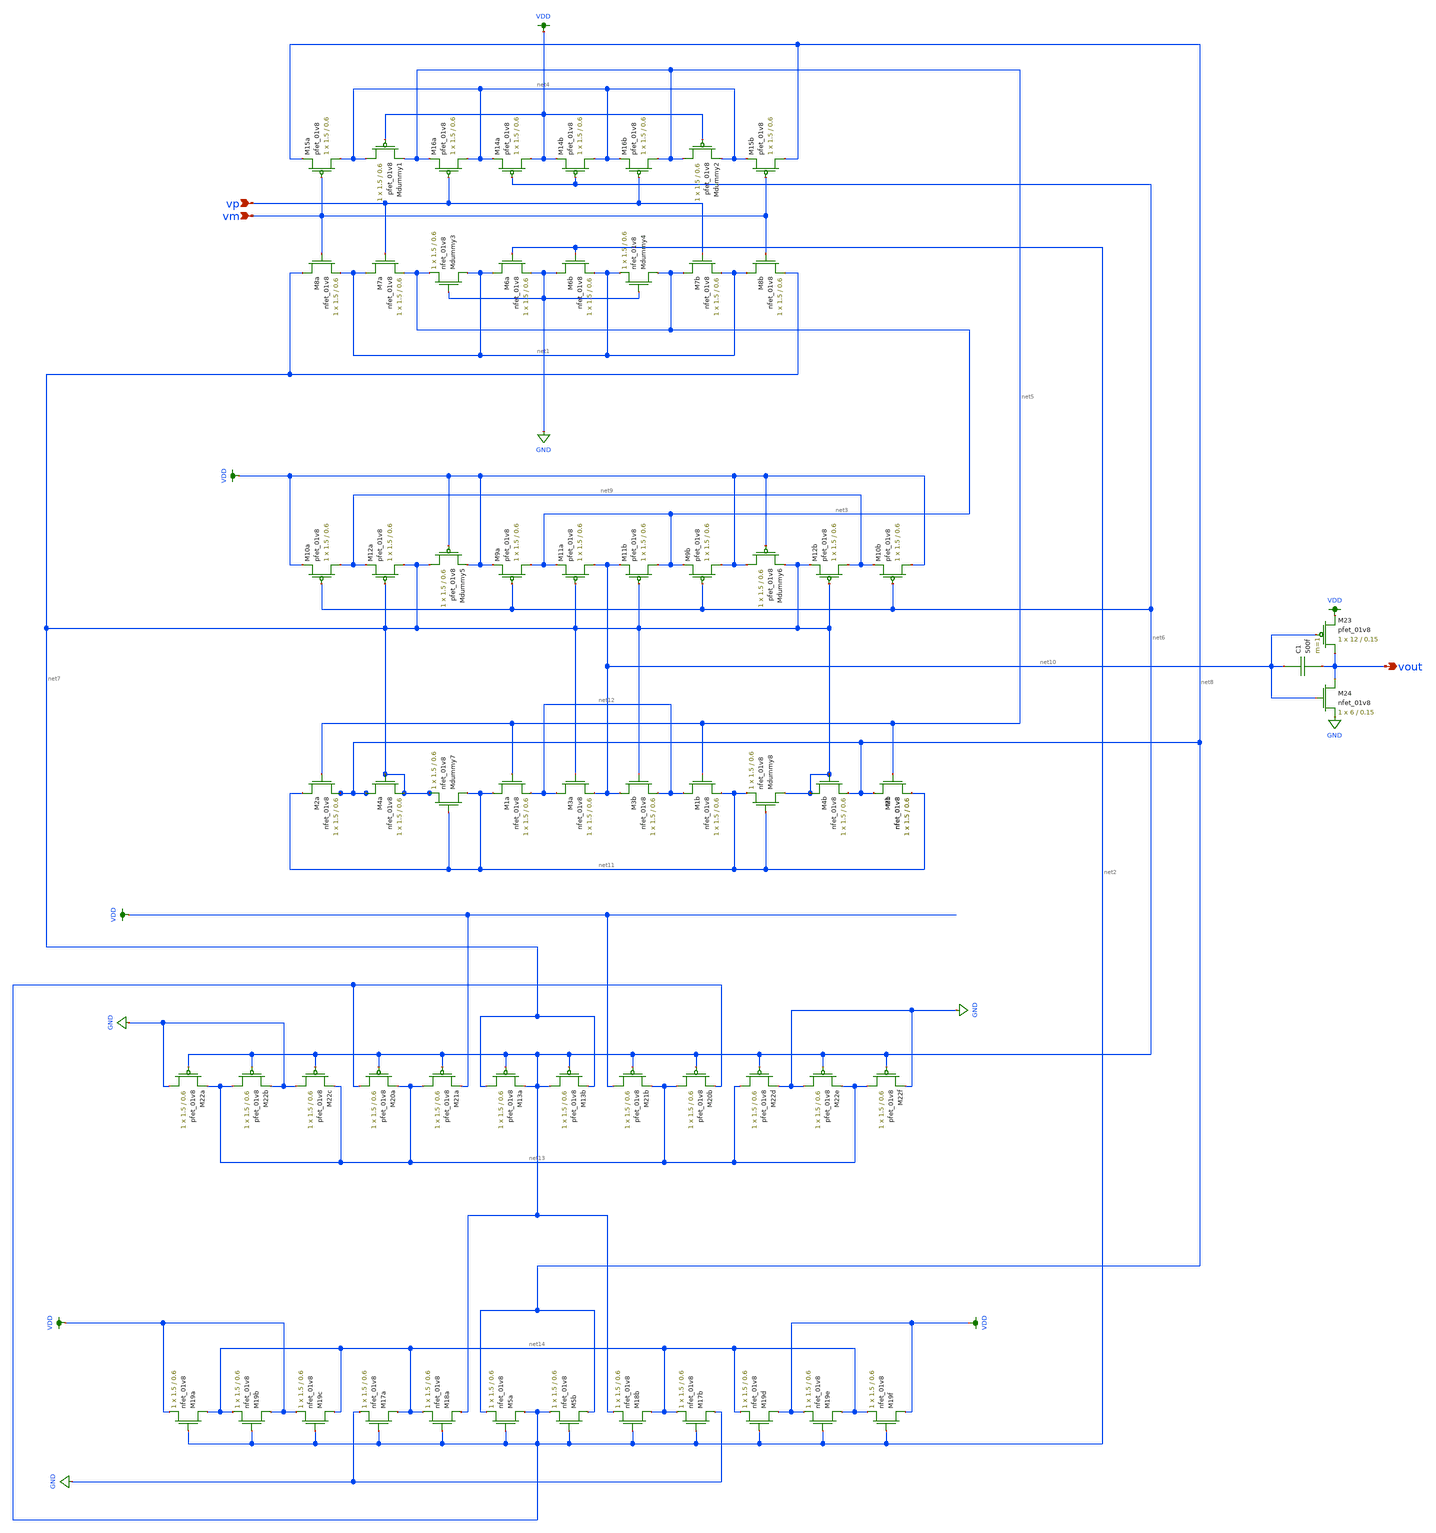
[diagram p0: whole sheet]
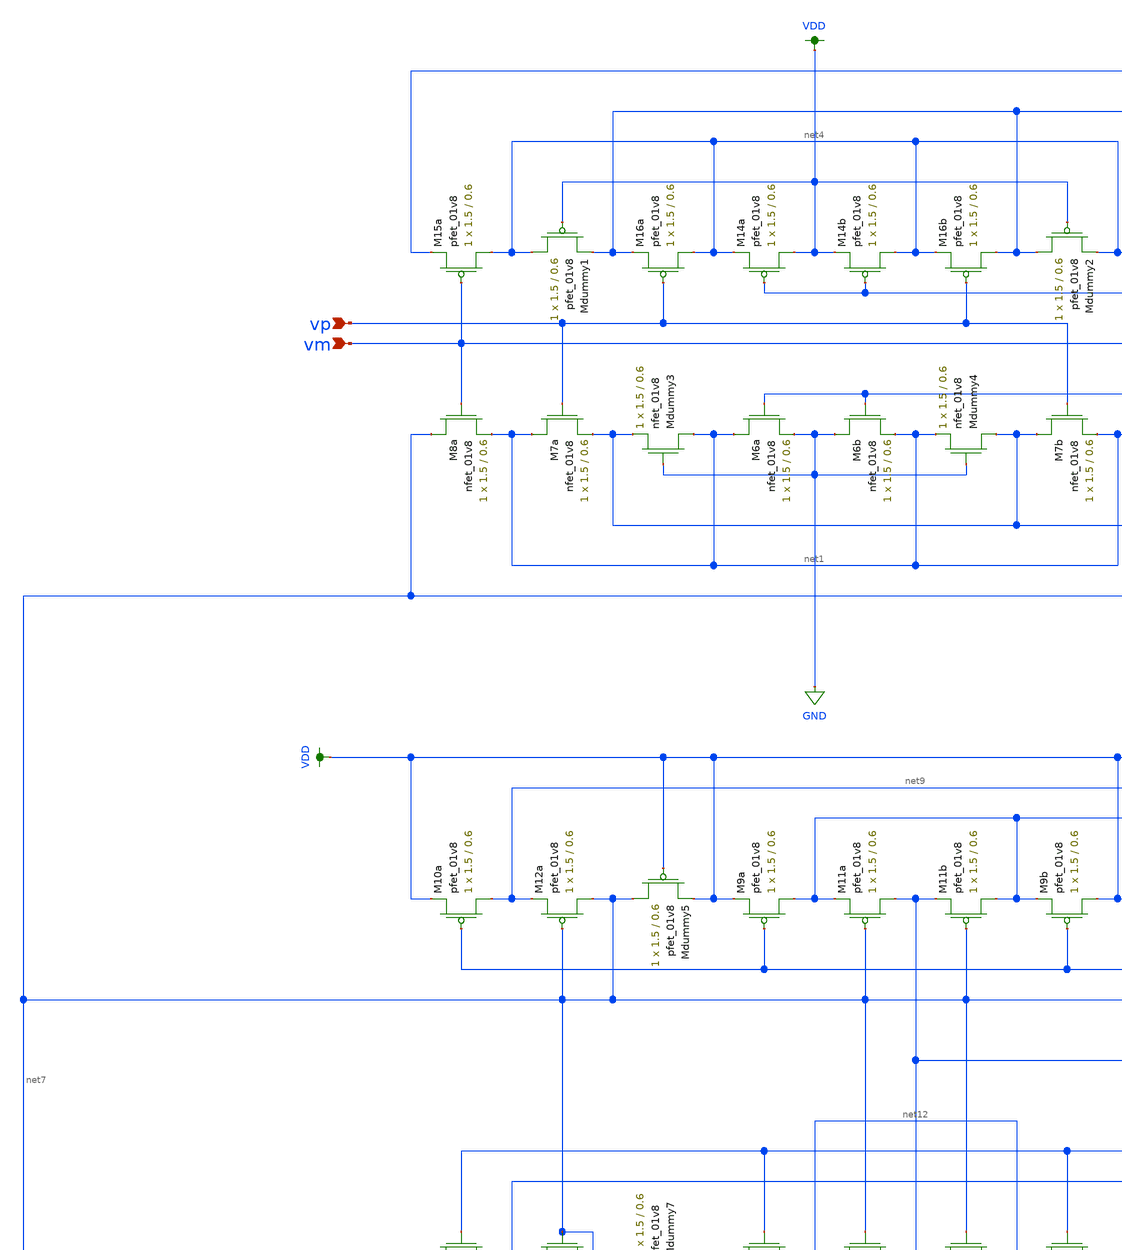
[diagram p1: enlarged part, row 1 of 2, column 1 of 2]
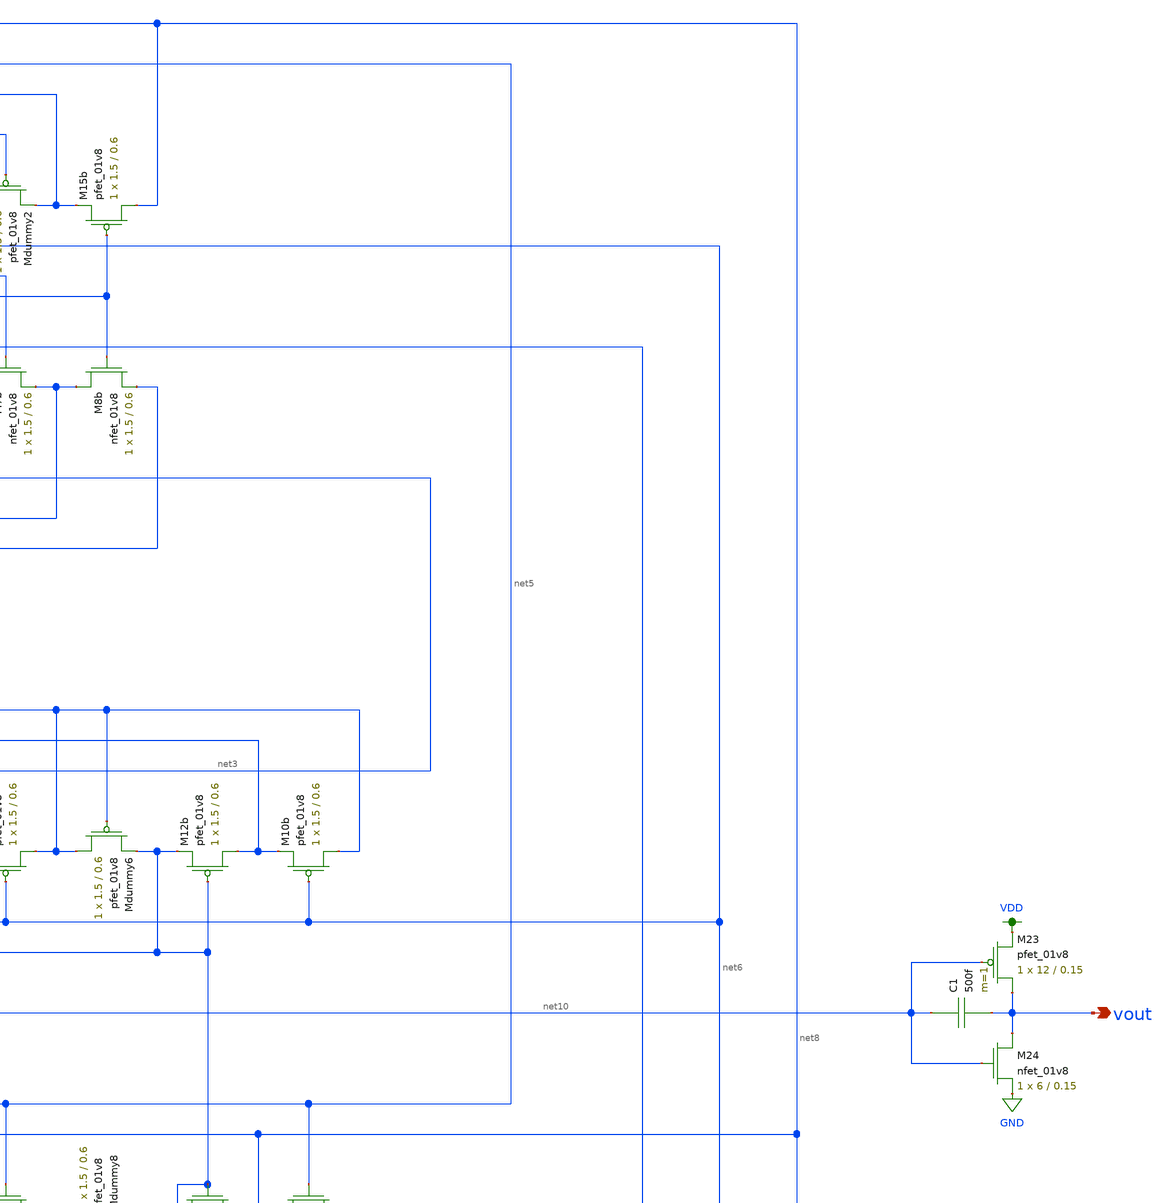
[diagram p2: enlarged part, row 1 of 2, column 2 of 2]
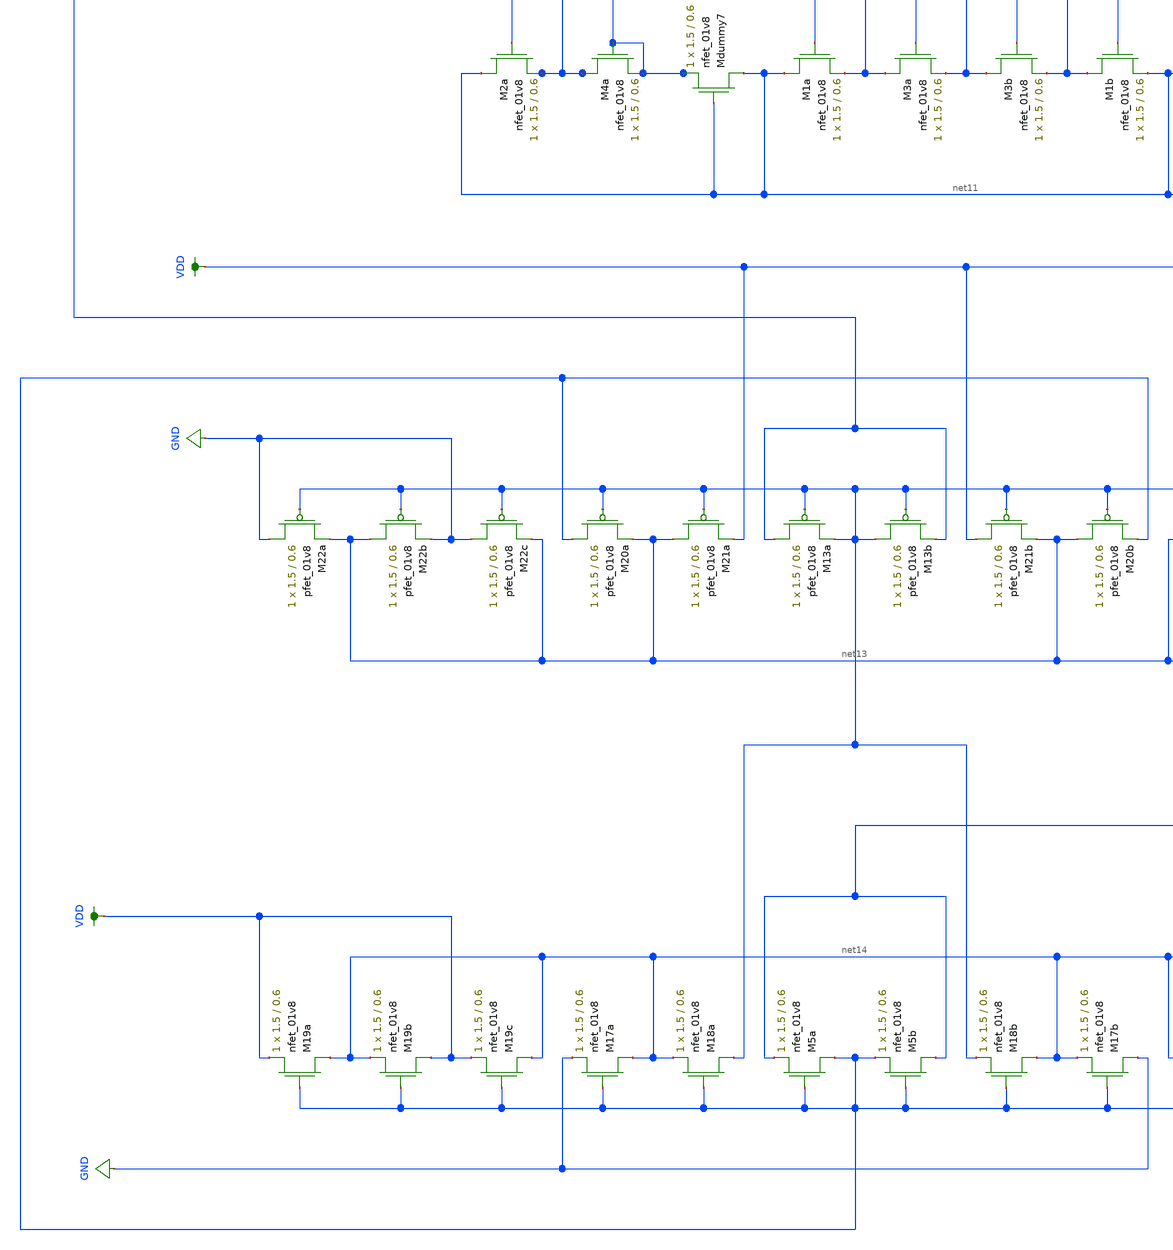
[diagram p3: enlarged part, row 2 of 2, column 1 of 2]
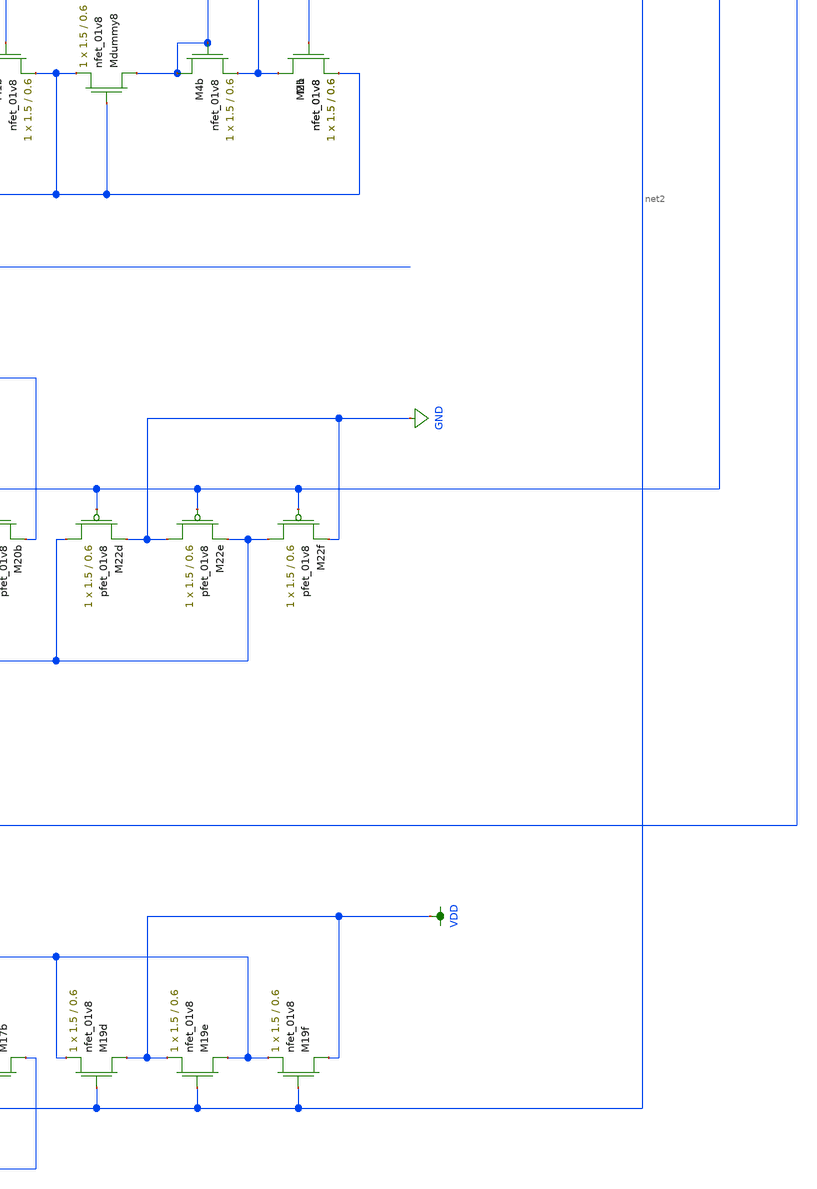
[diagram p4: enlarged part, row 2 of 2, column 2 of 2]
** sch_path: schematic/selfbiasedcascode2stage_lds.sch
**.subckt selfbiasedcascode2stage_lds vm vp vout
*.ipin vm
*.ipin vp
*.opin vout
XMdummy1 net4 VDD net5 VDD sky130_fd_pr__pfet_01v8 L=0.6 W=1.5 nf=1 ad='int((nf+1)/2) * W/nf * 0.29'
+ as='int((nf+2)/2) * W/nf * 0.29' pd='2*int((nf+1)/2) * (W/nf + 0.29)' ps='2*int((nf+2)/2) * (W/nf + 0.29)'
+ nrd='0.29 / W' nrs='0.29 / W' sa=0 sb=0 sd=0 mult=1 m=1
XM16a net4 vp net5 VDD sky130_fd_pr__pfet_01v8 L=0.6 W=1.5 nf=1 ad='int((nf+1)/2) * W/nf * 0.29' as='int((nf+2)/2) * W/nf * 0.29'
+ pd='2*int((nf+1)/2) * (W/nf + 0.29)' ps='2*int((nf+2)/2) * (W/nf + 0.29)' nrd='0.29 / W' nrs='0.29 / W'
+ sa=0 sb=0 sd=0 mult=1 m=1
XM14a VDD net6 net4 VDD sky130_fd_pr__pfet_01v8 L=0.6 W=1.5 nf=1 ad='int((nf+1)/2) * W/nf * 0.29' as='int((nf+2)/2) * W/nf * 0.29'
+ pd='2*int((nf+1)/2) * (W/nf + 0.29)' ps='2*int((nf+2)/2) * (W/nf + 0.29)' nrd='0.29 / W' nrs='0.29 / W'
+ sa=0 sb=0 sd=0 mult=1 m=1
XM14b net4 net6 VDD VDD sky130_fd_pr__pfet_01v8 L=0.6 W=1.5 nf=1 ad='int((nf+1)/2) * W/nf * 0.29' as='int((nf+2)/2) * W/nf * 0.29'
+ pd='2*int((nf+1)/2) * (W/nf + 0.29)' ps='2*int((nf+2)/2) * (W/nf + 0.29)' nrd='0.29 / W' nrs='0.29 / W'
+ sa=0 sb=0 sd=0 mult=1 m=1
XM15a net4 vm net8 VDD sky130_fd_pr__pfet_01v8 L=0.6 W=1.5 nf=1 ad='int((nf+1)/2) * W/nf * 0.29' as='int((nf+2)/2) * W/nf * 0.29'
+ pd='2*int((nf+1)/2) * (W/nf + 0.29)' ps='2*int((nf+2)/2) * (W/nf + 0.29)' nrd='0.29 / W' nrs='0.29 / W'
+ sa=0 sb=0 sd=0 mult=1 m=1
XM16b net5 vp net4 VDD sky130_fd_pr__pfet_01v8 L=0.6 W=1.5 nf=1 ad='int((nf+1)/2) * W/nf * 0.29' as='int((nf+2)/2) * W/nf * 0.29'
+ pd='2*int((nf+1)/2) * (W/nf + 0.29)' ps='2*int((nf+2)/2) * (W/nf + 0.29)' nrd='0.29 / W' nrs='0.29 / W'
+ sa=0 sb=0 sd=0 mult=1 m=1
XMdummy3 net1 GND net3 GND sky130_fd_pr__nfet_01v8 L=0.6 W=1.5 nf=1 ad='int((nf+1)/2) * W/nf * 0.29'
+ as='int((nf+2)/2) * W/nf * 0.29' pd='2*int((nf+1)/2) * (W/nf + 0.29)' ps='2*int((nf+2)/2) * (W/nf + 0.29)'
+ nrd='0.29 / W' nrs='0.29 / W' sa=0 sb=0 sd=0 mult=1 m=1
XM6a net1 net2 GND GND sky130_fd_pr__nfet_01v8 L=0.6 W=1.5 nf=1 ad='int((nf+1)/2) * W/nf * 0.29' as='int((nf+2)/2) * W/nf * 0.29'
+ pd='2*int((nf+1)/2) * (W/nf + 0.29)' ps='2*int((nf+2)/2) * (W/nf + 0.29)' nrd='0.29 / W' nrs='0.29 / W'
+ sa=0 sb=0 sd=0 mult=1 m=1
XM6b GND net2 net1 GND sky130_fd_pr__nfet_01v8 L=0.6 W=1.5 nf=1 ad='int((nf+1)/2) * W/nf * 0.29' as='int((nf+2)/2) * W/nf * 0.29'
+ pd='2*int((nf+1)/2) * (W/nf + 0.29)' ps='2*int((nf+2)/2) * (W/nf + 0.29)' nrd='0.29 / W' nrs='0.29 / W'
+ sa=0 sb=0 sd=0 mult=1 m=1
XMdummy4 net3 GND net1 GND sky130_fd_pr__nfet_01v8 L=0.6 W=1.5 nf=1 ad='int((nf+1)/2) * W/nf * 0.29'
+ as='int((nf+2)/2) * W/nf * 0.29' pd='2*int((nf+1)/2) * (W/nf + 0.29)' ps='2*int((nf+2)/2) * (W/nf + 0.29)'
+ nrd='0.29 / W' nrs='0.29 / W' sa=0 sb=0 sd=0 mult=1 m=1
XM8a net7 vm net1 GND sky130_fd_pr__nfet_01v8 L=0.6 W=1.5 nf=1 ad='int((nf+1)/2) * W/nf * 0.29' as='int((nf+2)/2) * W/nf * 0.29'
+ pd='2*int((nf+1)/2) * (W/nf + 0.29)' ps='2*int((nf+2)/2) * (W/nf + 0.29)' nrd='0.29 / W' nrs='0.29 / W'
+ sa=0 sb=0 sd=0 mult=1 m=1
XM7a net1 vp net3 GND sky130_fd_pr__nfet_01v8 L=0.6 W=1.5 nf=1 ad='int((nf+1)/2) * W/nf * 0.29' as='int((nf+2)/2) * W/nf * 0.29'
+ pd='2*int((nf+1)/2) * (W/nf + 0.29)' ps='2*int((nf+2)/2) * (W/nf + 0.29)' nrd='0.29 / W' nrs='0.29 / W'
+ sa=0 sb=0 sd=0 mult=1 m=1
XMdummy2 net5 VDD net4 VDD sky130_fd_pr__pfet_01v8 L=0.6 W=1.5 nf=1 ad='int((nf+1)/2) * W/nf * 0.29'
+ as='int((nf+2)/2) * W/nf * 0.29' pd='2*int((nf+1)/2) * (W/nf + 0.29)' ps='2*int((nf+2)/2) * (W/nf + 0.29)'
+ nrd='0.29 / W' nrs='0.29 / W' sa=0 sb=0 sd=0 mult=1 m=1
XM15b net8 vm net4 VDD sky130_fd_pr__pfet_01v8 L=0.6 W=1.5 nf=1 ad='int((nf+1)/2) * W/nf * 0.29' as='int((nf+2)/2) * W/nf * 0.29'
+ pd='2*int((nf+1)/2) * (W/nf + 0.29)' ps='2*int((nf+2)/2) * (W/nf + 0.29)' nrd='0.29 / W' nrs='0.29 / W'
+ sa=0 sb=0 sd=0 mult=1 m=1
XM7b net3 vp net1 GND sky130_fd_pr__nfet_01v8 L=0.6 W=1.5 nf=1 ad='int((nf+1)/2) * W/nf * 0.29' as='int((nf+2)/2) * W/nf * 0.29'
+ pd='2*int((nf+1)/2) * (W/nf + 0.29)' ps='2*int((nf+2)/2) * (W/nf + 0.29)' nrd='0.29 / W' nrs='0.29 / W'
+ sa=0 sb=0 sd=0 mult=1 m=1
XM8b net1 vm net7 GND sky130_fd_pr__nfet_01v8 L=0.6 W=1.5 nf=1 ad='int((nf+1)/2) * W/nf * 0.29' as='int((nf+2)/2) * W/nf * 0.29'
+ pd='2*int((nf+1)/2) * (W/nf + 0.29)' ps='2*int((nf+2)/2) * (W/nf + 0.29)' nrd='0.29 / W' nrs='0.29 / W'
+ sa=0 sb=0 sd=0 mult=1 m=1
XM10a net9 net6 VDD VDD sky130_fd_pr__pfet_01v8 L=0.6 W=1.5 nf=1 ad='int((nf+1)/2) * W/nf * 0.29' as='int((nf+2)/2) * W/nf * 0.29'
+ pd='2*int((nf+1)/2) * (W/nf + 0.29)' ps='2*int((nf+2)/2) * (W/nf + 0.29)' nrd='0.29 / W' nrs='0.29 / W'
+ sa=0 sb=0 sd=0 mult=1 m=1
XM9a net3 net6 VDD VDD sky130_fd_pr__pfet_01v8 L=0.6 W=1.5 nf=1 ad='int((nf+1)/2) * W/nf * 0.29' as='int((nf+2)/2) * W/nf * 0.29'
+ pd='2*int((nf+1)/2) * (W/nf + 0.29)' ps='2*int((nf+2)/2) * (W/nf + 0.29)' nrd='0.29 / W' nrs='0.29 / W'
+ sa=0 sb=0 sd=0 mult=1 m=1
XM12a net7 net7 net9 VDD sky130_fd_pr__pfet_01v8 L=0.6 W=1.5 nf=1 ad='int((nf+1)/2) * W/nf * 0.29' as='int((nf+2)/2) * W/nf * 0.29'
+ pd='2*int((nf+1)/2) * (W/nf + 0.29)' ps='2*int((nf+2)/2) * (W/nf + 0.29)' nrd='0.29 / W' nrs='0.29 / W'
+ sa=0 sb=0 sd=0 mult=1 m=1
XM11a net10 net7 net3 VDD sky130_fd_pr__pfet_01v8 L=0.6 W=1.5 nf=1 ad='int((nf+1)/2) * W/nf * 0.29' as='int((nf+2)/2) * W/nf * 0.29'
+ pd='2*int((nf+1)/2) * (W/nf + 0.29)' ps='2*int((nf+2)/2) * (W/nf + 0.29)' nrd='0.29 / W' nrs='0.29 / W'
+ sa=0 sb=0 sd=0 mult=1 m=1
XM11b net3 net7 net10 VDD sky130_fd_pr__pfet_01v8 L=0.6 W=1.5 nf=1 ad='int((nf+1)/2) * W/nf * 0.29' as='int((nf+2)/2) * W/nf * 0.29'
+ pd='2*int((nf+1)/2) * (W/nf + 0.29)' ps='2*int((nf+2)/2) * (W/nf + 0.29)' nrd='0.29 / W' nrs='0.29 / W'
+ sa=0 sb=0 sd=0 mult=1 m=1
XM12b net9 net7 net7 VDD sky130_fd_pr__pfet_01v8 L=0.6 W=1.5 nf=1 ad='int((nf+1)/2) * W/nf * 0.29' as='int((nf+2)/2) * W/nf * 0.29'
+ pd='2*int((nf+1)/2) * (W/nf + 0.29)' ps='2*int((nf+2)/2) * (W/nf + 0.29)' nrd='0.29 / W' nrs='0.29 / W'
+ sa=0 sb=0 sd=0 mult=1 m=1
XM9b VDD net6 net3 VDD sky130_fd_pr__pfet_01v8 L=0.6 W=1.5 nf=1 ad='int((nf+1)/2) * W/nf * 0.29' as='int((nf+2)/2) * W/nf * 0.29'
+ pd='2*int((nf+1)/2) * (W/nf + 0.29)' ps='2*int((nf+2)/2) * (W/nf + 0.29)' nrd='0.29 / W' nrs='0.29 / W'
+ sa=0 sb=0 sd=0 mult=1 m=1
XM10b VDD net6 net9 VDD sky130_fd_pr__pfet_01v8 L=0.6 W=1.5 nf=1 ad='int((nf+1)/2) * W/nf * 0.29' as='int((nf+2)/2) * W/nf * 0.29'
+ pd='2*int((nf+1)/2) * (W/nf + 0.29)' ps='2*int((nf+2)/2) * (W/nf + 0.29)' nrd='0.29 / W' nrs='0.29 / W'
+ sa=0 sb=0 sd=0 mult=1 m=1
XMdummy5 net7 VDD VDD VDD sky130_fd_pr__pfet_01v8 L=0.6 W=1.5 nf=1 ad='int((nf+1)/2) * W/nf * 0.29' as='int((nf+2)/2) * W/nf * 0.29'
+ pd='2*int((nf+1)/2) * (W/nf + 0.29)' ps='2*int((nf+2)/2) * (W/nf + 0.29)' nrd='0.29 / W' nrs='0.29 / W'
+ sa=0 sb=0 sd=0 mult=1 m=1
XMdummy6 VDD VDD net7 VDD sky130_fd_pr__pfet_01v8 L=0.6 W=1.5 nf=1 ad='int((nf+1)/2) * W/nf * 0.29' as='int((nf+2)/2) * W/nf * 0.29'
+ pd='2*int((nf+1)/2) * (W/nf + 0.29)' ps='2*int((nf+2)/2) * (W/nf + 0.29)' nrd='0.29 / W' nrs='0.29 / W'
+ sa=0 sb=0 sd=0 mult=1 m=1
XM2a net11 net5 net8 GND sky130_fd_pr__nfet_01v8 L=0.6 W=1.5 nf=1 ad='int((nf+1)/2) * W/nf * 0.29' as='int((nf+2)/2) * W/nf * 0.29'
+ pd='2*int((nf+1)/2) * (W/nf + 0.29)' ps='2*int((nf+2)/2) * (W/nf + 0.29)' nrd='0.29 / W' nrs='0.29 / W'
+ sa=0 sb=0 sd=0 mult=1 m=1
XM4a net8 net7 net7 GND sky130_fd_pr__nfet_01v8 L=0.6 W=1.5 nf=1 ad='int((nf+1)/2) * W/nf * 0.29' as='int((nf+2)/2) * W/nf * 0.29'
+ pd='2*int((nf+1)/2) * (W/nf + 0.29)' ps='2*int((nf+2)/2) * (W/nf + 0.29)' nrd='0.29 / W' nrs='0.29 / W'
+ sa=0 sb=0 sd=0 mult=1 m=1
XMdummy7 net11 net11 net7 GND sky130_fd_pr__nfet_01v8 L=0.6 W=1.5 nf=1 ad='int((nf+1)/2) * W/nf * 0.29'
+ as='int((nf+2)/2) * W/nf * 0.29' pd='2*int((nf+1)/2) * (W/nf + 0.29)' ps='2*int((nf+2)/2) * (W/nf + 0.29)'
+ nrd='0.29 / W' nrs='0.29 / W' sa=0 sb=0 sd=0 mult=1 m=1
XM1a net11 net5 net12 GND sky130_fd_pr__nfet_01v8 L=0.6 W=1.5 nf=1 ad='int((nf+1)/2) * W/nf * 0.29' as='int((nf+2)/2) * W/nf * 0.29'
+ pd='2*int((nf+1)/2) * (W/nf + 0.29)' ps='2*int((nf+2)/2) * (W/nf + 0.29)' nrd='0.29 / W' nrs='0.29 / W'
+ sa=0 sb=0 sd=0 mult=1 m=1
XM3a net12 net7 net10 GND sky130_fd_pr__nfet_01v8 L=0.6 W=1.5 nf=1 ad='int((nf+1)/2) * W/nf * 0.29' as='int((nf+2)/2) * W/nf * 0.29'
+ pd='2*int((nf+1)/2) * (W/nf + 0.29)' ps='2*int((nf+2)/2) * (W/nf + 0.29)' nrd='0.29 / W' nrs='0.29 / W'
+ sa=0 sb=0 sd=0 mult=1 m=1
XM3b net10 net7 net12 GND sky130_fd_pr__nfet_01v8 L=0.6 W=1.5 nf=1 ad='int((nf+1)/2) * W/nf * 0.29' as='int((nf+2)/2) * W/nf * 0.29'
+ pd='2*int((nf+1)/2) * (W/nf + 0.29)' ps='2*int((nf+2)/2) * (W/nf + 0.29)' nrd='0.29 / W' nrs='0.29 / W'
+ sa=0 sb=0 sd=0 mult=1 m=1
XM1b net12 net5 net11 GND sky130_fd_pr__nfet_01v8 L=0.6 W=1.5 nf=1 ad='int((nf+1)/2) * W/nf * 0.29' as='int((nf+2)/2) * W/nf * 0.29'
+ pd='2*int((nf+1)/2) * (W/nf + 0.29)' ps='2*int((nf+2)/2) * (W/nf + 0.29)' nrd='0.29 / W' nrs='0.29 / W'
+ sa=0 sb=0 sd=0 mult=1 m=1
XMdummy8 net7 net11 net11 GND sky130_fd_pr__nfet_01v8 L=0.6 W=1.5 nf=1 ad='int((nf+1)/2) * W/nf * 0.29'
+ as='int((nf+2)/2) * W/nf * 0.29' pd='2*int((nf+1)/2) * (W/nf + 0.29)' ps='2*int((nf+2)/2) * (W/nf + 0.29)'
+ nrd='0.29 / W' nrs='0.29 / W' sa=0 sb=0 sd=0 mult=1 m=1
XM4b net7 net7 net8 GND sky130_fd_pr__nfet_01v8 L=0.6 W=1.5 nf=1 ad='int((nf+1)/2) * W/nf * 0.29' as='int((nf+2)/2) * W/nf * 0.29'
+ pd='2*int((nf+1)/2) * (W/nf + 0.29)' ps='2*int((nf+2)/2) * (W/nf + 0.29)' nrd='0.29 / W' nrs='0.29 / W'
+ sa=0 sb=0 sd=0 mult=1 m=1
XM2b net8 net5 net11 GND sky130_fd_pr__nfet_01v8 L=0.6 W=1.5 nf=1 ad='int((nf+1)/2) * W/nf * 0.29' as='int((nf+2)/2) * W/nf * 0.29'
+ pd='2*int((nf+1)/2) * (W/nf + 0.29)' ps='2*int((nf+2)/2) * (W/nf + 0.29)' nrd='0.29 / W' nrs='0.29 / W'
+ sa=0 sb=0 sd=0 mult=1 m=1
XM13a net7 net6 net6 VDD sky130_fd_pr__pfet_01v8 L=0.6 W=1.5 nf=1 ad='int((nf+1)/2) * W/nf * 0.29' as='int((nf+2)/2) * W/nf * 0.29'
+ pd='2*int((nf+1)/2) * (W/nf + 0.29)' ps='2*int((nf+2)/2) * (W/nf + 0.29)' nrd='0.29 / W' nrs='0.29 / W'
+ sa=0 sb=0 sd=0 mult=1 m=1
XM21a net13 net6 VDD VDD sky130_fd_pr__pfet_01v8 L=0.6 W=1.5 nf=1 ad='int((nf+1)/2) * W/nf * 0.29' as='int((nf+2)/2) * W/nf * 0.29'
+ pd='2*int((nf+1)/2) * (W/nf + 0.29)' ps='2*int((nf+2)/2) * (W/nf + 0.29)' nrd='0.29 / W' nrs='0.29 / W'
+ sa=0 sb=0 sd=0 mult=1 m=1
XM22c GND net6 net13 VDD sky130_fd_pr__pfet_01v8 L=0.6 W=1.5 nf=1 ad='int((nf+1)/2) * W/nf * 0.29' as='int((nf+2)/2) * W/nf * 0.29'
+ pd='2*int((nf+1)/2) * (W/nf + 0.29)' ps='2*int((nf+2)/2) * (W/nf + 0.29)' nrd='0.29 / W' nrs='0.29 / W'
+ sa=0 sb=0 sd=0 mult=1 m=1
XM20a net2 net6 net13 VDD sky130_fd_pr__pfet_01v8 L=0.6 W=1.5 nf=1 ad='int((nf+1)/2) * W/nf * 0.29' as='int((nf+2)/2) * W/nf * 0.29'
+ pd='2*int((nf+1)/2) * (W/nf + 0.29)' ps='2*int((nf+2)/2) * (W/nf + 0.29)' nrd='0.29 / W' nrs='0.29 / W'
+ sa=0 sb=0 sd=0 mult=1 m=1
XM22a GND net6 net13 VDD sky130_fd_pr__pfet_01v8 L=0.6 W=1.5 nf=1 ad='int((nf+1)/2) * W/nf * 0.29' as='int((nf+2)/2) * W/nf * 0.29'
+ pd='2*int((nf+1)/2) * (W/nf + 0.29)' ps='2*int((nf+2)/2) * (W/nf + 0.29)' nrd='0.29 / W' nrs='0.29 / W'
+ sa=0 sb=0 sd=0 mult=1 m=1
XM22b net13 net6 GND VDD sky130_fd_pr__pfet_01v8 L=0.6 W=1.5 nf=1 ad='int((nf+1)/2) * W/nf * 0.29' as='int((nf+2)/2) * W/nf * 0.29'
+ pd='2*int((nf+1)/2) * (W/nf + 0.29)' ps='2*int((nf+2)/2) * (W/nf + 0.29)' nrd='0.29 / W' nrs='0.29 / W'
+ sa=0 sb=0 sd=0 mult=1 m=1
XM22f net13 net6 GND VDD sky130_fd_pr__pfet_01v8 L=0.6 W=1.5 nf=1 ad='int((nf+1)/2) * W/nf * 0.29' as='int((nf+2)/2) * W/nf * 0.29'
+ pd='2*int((nf+1)/2) * (W/nf + 0.29)' ps='2*int((nf+2)/2) * (W/nf + 0.29)' nrd='0.29 / W' nrs='0.29 / W'
+ sa=0 sb=0 sd=0 mult=1 m=1
XM22e GND net6 net13 VDD sky130_fd_pr__pfet_01v8 L=0.6 W=1.5 nf=1 ad='int((nf+1)/2) * W/nf * 0.29' as='int((nf+2)/2) * W/nf * 0.29'
+ pd='2*int((nf+1)/2) * (W/nf + 0.29)' ps='2*int((nf+2)/2) * (W/nf + 0.29)' nrd='0.29 / W' nrs='0.29 / W'
+ sa=0 sb=0 sd=0 mult=1 m=1
XM20b net13 net6 net2 VDD sky130_fd_pr__pfet_01v8 L=0.6 W=1.5 nf=1 ad='int((nf+1)/2) * W/nf * 0.29' as='int((nf+2)/2) * W/nf * 0.29'
+ pd='2*int((nf+1)/2) * (W/nf + 0.29)' ps='2*int((nf+2)/2) * (W/nf + 0.29)' nrd='0.29 / W' nrs='0.29 / W'
+ sa=0 sb=0 sd=0 mult=1 m=1
XM22d net13 net6 GND VDD sky130_fd_pr__pfet_01v8 L=0.6 W=1.5 nf=1 ad='int((nf+1)/2) * W/nf * 0.29' as='int((nf+2)/2) * W/nf * 0.29'
+ pd='2*int((nf+1)/2) * (W/nf + 0.29)' ps='2*int((nf+2)/2) * (W/nf + 0.29)' nrd='0.29 / W' nrs='0.29 / W'
+ sa=0 sb=0 sd=0 mult=1 m=1
XM13b net6 net6 net7 VDD sky130_fd_pr__pfet_01v8 L=0.6 W=1.5 nf=1 ad='int((nf+1)/2) * W/nf * 0.29' as='int((nf+2)/2) * W/nf * 0.29'
+ pd='2*int((nf+1)/2) * (W/nf + 0.29)' ps='2*int((nf+2)/2) * (W/nf + 0.29)' nrd='0.29 / W' nrs='0.29 / W'
+ sa=0 sb=0 sd=0 mult=1 m=1
XM21b VDD net6 net13 VDD sky130_fd_pr__pfet_01v8 L=0.6 W=1.5 nf=1 ad='int((nf+1)/2) * W/nf * 0.29' as='int((nf+2)/2) * W/nf * 0.29'
+ pd='2*int((nf+1)/2) * (W/nf + 0.29)' ps='2*int((nf+2)/2) * (W/nf + 0.29)' nrd='0.29 / W' nrs='0.29 / W'
+ sa=0 sb=0 sd=0 mult=1 m=1
XM5a net2 net2 net8 GND sky130_fd_pr__nfet_01v8 L=0.6 W=1.5 nf=1 ad='int((nf+1)/2) * W/nf * 0.29' as='int((nf+2)/2) * W/nf * 0.29'
+ pd='2*int((nf+1)/2) * (W/nf + 0.29)' ps='2*int((nf+2)/2) * (W/nf + 0.29)' nrd='0.29 / W' nrs='0.29 / W'
+ sa=0 sb=0 sd=0 mult=1 m=1
XM18a net6 net2 net14 GND sky130_fd_pr__nfet_01v8 L=0.6 W=1.5 nf=1 ad='int((nf+1)/2) * W/nf * 0.29' as='int((nf+2)/2) * W/nf * 0.29'
+ pd='2*int((nf+1)/2) * (W/nf + 0.29)' ps='2*int((nf+2)/2) * (W/nf + 0.29)' nrd='0.29 / W' nrs='0.29 / W'
+ sa=0 sb=0 sd=0 mult=1 m=1
XM17a net14 net2 GND GND sky130_fd_pr__nfet_01v8 L=0.6 W=1.5 nf=1 ad='int((nf+1)/2) * W/nf * 0.29' as='int((nf+2)/2) * W/nf * 0.29'
+ pd='2*int((nf+1)/2) * (W/nf + 0.29)' ps='2*int((nf+2)/2) * (W/nf + 0.29)' nrd='0.29 / W' nrs='0.29 / W'
+ sa=0 sb=0 sd=0 mult=1 m=1
XM19c net14 net2 VDD GND sky130_fd_pr__nfet_01v8 L=0.6 W=1.5 nf=1 ad='int((nf+1)/2) * W/nf * 0.29' as='int((nf+2)/2) * W/nf * 0.29'
+ pd='2*int((nf+1)/2) * (W/nf + 0.29)' ps='2*int((nf+2)/2) * (W/nf + 0.29)' nrd='0.29 / W' nrs='0.29 / W'
+ sa=0 sb=0 sd=0 mult=1 m=1
XM19b VDD net2 net14 GND sky130_fd_pr__nfet_01v8 L=0.6 W=1.5 nf=1 ad='int((nf+1)/2) * W/nf * 0.29' as='int((nf+2)/2) * W/nf * 0.29'
+ pd='2*int((nf+1)/2) * (W/nf + 0.29)' ps='2*int((nf+2)/2) * (W/nf + 0.29)' nrd='0.29 / W' nrs='0.29 / W'
+ sa=0 sb=0 sd=0 mult=1 m=1
XM19a net14 net2 VDD GND sky130_fd_pr__nfet_01v8 L=0.6 W=1.5 nf=1 ad='int((nf+1)/2) * W/nf * 0.29' as='int((nf+2)/2) * W/nf * 0.29'
+ pd='2*int((nf+1)/2) * (W/nf + 0.29)' ps='2*int((nf+2)/2) * (W/nf + 0.29)' nrd='0.29 / W' nrs='0.29 / W'
+ sa=0 sb=0 sd=0 mult=1 m=1
XM19f VDD net2 net14 GND sky130_fd_pr__nfet_01v8 L=0.6 W=1.5 nf=1 ad='int((nf+1)/2) * W/nf * 0.29' as='int((nf+2)/2) * W/nf * 0.29'
+ pd='2*int((nf+1)/2) * (W/nf + 0.29)' ps='2*int((nf+2)/2) * (W/nf + 0.29)' nrd='0.29 / W' nrs='0.29 / W'
+ sa=0 sb=0 sd=0 mult=1 m=1
XM19e net14 net2 VDD GND sky130_fd_pr__nfet_01v8 L=0.6 W=1.5 nf=1 ad='int((nf+1)/2) * W/nf * 0.29' as='int((nf+2)/2) * W/nf * 0.29'
+ pd='2*int((nf+1)/2) * (W/nf + 0.29)' ps='2*int((nf+2)/2) * (W/nf + 0.29)' nrd='0.29 / W' nrs='0.29 / W'
+ sa=0 sb=0 sd=0 mult=1 m=1
XM19d VDD net2 net14 GND sky130_fd_pr__nfet_01v8 L=0.6 W=1.5 nf=1 ad='int((nf+1)/2) * W/nf * 0.29' as='int((nf+2)/2) * W/nf * 0.29'
+ pd='2*int((nf+1)/2) * (W/nf + 0.29)' ps='2*int((nf+2)/2) * (W/nf + 0.29)' nrd='0.29 / W' nrs='0.29 / W'
+ sa=0 sb=0 sd=0 mult=1 m=1
XM17b GND net2 net14 GND sky130_fd_pr__nfet_01v8 L=0.6 W=1.5 nf=1 ad='int((nf+1)/2) * W/nf * 0.29' as='int((nf+2)/2) * W/nf * 0.29'
+ pd='2*int((nf+1)/2) * (W/nf + 0.29)' ps='2*int((nf+2)/2) * (W/nf + 0.29)' nrd='0.29 / W' nrs='0.29 / W'
+ sa=0 sb=0 sd=0 mult=1 m=1
XM18b net14 net2 net6 GND sky130_fd_pr__nfet_01v8 L=0.6 W=1.5 nf=1 ad='int((nf+1)/2) * W/nf * 0.29' as='int((nf+2)/2) * W/nf * 0.29'
+ pd='2*int((nf+1)/2) * (W/nf + 0.29)' ps='2*int((nf+2)/2) * (W/nf + 0.29)' nrd='0.29 / W' nrs='0.29 / W'
+ sa=0 sb=0 sd=0 mult=1 m=1
XM5b net8 net2 net2 GND sky130_fd_pr__nfet_01v8 L=0.6 W=1.5 nf=1 ad='int((nf+1)/2) * W/nf * 0.29' as='int((nf+2)/2) * W/nf * 0.29'
+ pd='2*int((nf+1)/2) * (W/nf + 0.29)' ps='2*int((nf+2)/2) * (W/nf + 0.29)' nrd='0.29 / W' nrs='0.29 / W'
+ sa=0 sb=0 sd=0 mult=1 m=1
XM23 vout net10 VDD VDD sky130_fd_pr__pfet_01v8 L=0.15 W=12 nf=1 ad='int((nf+1)/2) * W/nf * 0.29' as='int((nf+2)/2) * W/nf * 0.29'
+ pd='2*int((nf+1)/2) * (W/nf + 0.29)' ps='2*int((nf+2)/2) * (W/nf + 0.29)' nrd='0.29 / W' nrs='0.29 / W'
+ sa=0 sb=0 sd=0 mult=1 m=1
XM24 vout net10 GND GND sky130_fd_pr__nfet_01v8 L=0.15 W=6 nf=1 ad='int((nf+1)/2) * W/nf * 0.29' as='int((nf+2)/2) * W/nf * 0.29'
+ pd='2*int((nf+1)/2) * (W/nf + 0.29)' ps='2*int((nf+2)/2) * (W/nf + 0.29)' nrd='0.29 / W' nrs='0.29 / W'
+ sa=0 sb=0 sd=0 mult=1 m=1
C1 net10 vout 500f m=1
XM1 net8 net5 net11 GND sky130_fd_pr__nfet_01v8 L=0.6 W=1.5 nf=1 ad='int((nf+1)/2) * W/nf * 0.29' as='int((nf+2)/2) * W/nf * 0.29'
+ pd='2*int((nf+1)/2) * (W/nf + 0.29)' ps='2*int((nf+2)/2) * (W/nf + 0.29)' nrd='0.29 / W' nrs='0.29 / W'
+ sa=0 sb=0 sd=0 mult=1 m=1
**.ends
.GLOBAL VDD
.GLOBAL GND
.end
